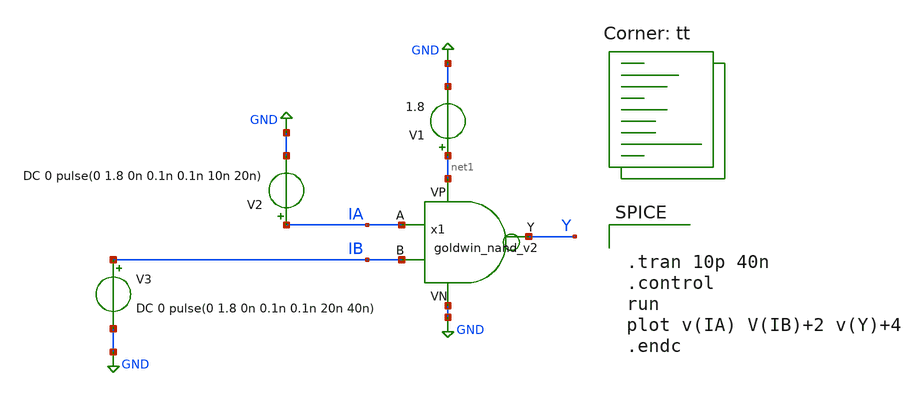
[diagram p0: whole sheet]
** sch_path: APIC-UTS/schematic/goldwin_nand_v2/tb_goldwin_nand_v2.sch
**.subckt tb_goldwin_nand_v2
V1 net1 GND 1.8
V2 IA GND DC 0 pulse(0 1.8 0n 0.1n 0.1n 10n 20n)
V3 IB GND DC 0 pulse(0 1.8 0n 0.1n 0.1n 20n 40n)
x1 IA IB Y net1 GND goldwin_nand_v2
**** begin user architecture code


.tran 10p 40n
.control
run
plot v(IA) V(IB)+2 v(Y)+4
.endc


.lib $::SKYWATER_MODELS/sky130.lib.spice tt
**** end user architecture code
**.ends

* expanding   symbol:  goldwin_nand_v2.sym # of pins=5
** sym_path: APIC-UTS/schematic/goldwin_nand_v2/goldwin_nand_v2.sym
** sch_path: APIC-UTS/schematic/goldwin_nand_v2/goldwin_nand_v2.sch
.subckt goldwin_nand_v2 A B Y VP VN
*.ipin A
*.ipin B
*.ipin VP
*.ipin VN
*.opin Y
XM1 Y A VP VP sky130_fd_pr__pfet_01v8 L=0.15 W=3 nf=1 ad='int((nf+1)/2) * W/nf * 0.29' as='int((nf+2)/2) * W/nf * 0.29'
+ pd='2*int((nf+1)/2) * (W/nf + 0.29)' ps='2*int((nf+2)/2) * (W/nf + 0.29)' nrd='0.29 / W' nrs='0.29 / W'
+ sa=0 sb=0 sd=0 mult=1 m=1
XM2 Y B VP VP sky130_fd_pr__pfet_01v8 L=0.15 W=3 nf=1 ad='int((nf+1)/2) * W/nf * 0.29' as='int((nf+2)/2) * W/nf * 0.29'
+ pd='2*int((nf+1)/2) * (W/nf + 0.29)' ps='2*int((nf+2)/2) * (W/nf + 0.29)' nrd='0.29 / W' nrs='0.29 / W'
+ sa=0 sb=0 sd=0 mult=1 m=1
XM3 Y B net1 VN sky130_fd_pr__nfet_01v8 L=0.15 W=1 nf=1 ad='int((nf+1)/2) * W/nf * 0.29' as='int((nf+2)/2) * W/nf * 0.29'
+ pd='2*int((nf+1)/2) * (W/nf + 0.29)' ps='2*int((nf+2)/2) * (W/nf + 0.29)' nrd='0.29 / W' nrs='0.29 / W'
+ sa=0 sb=0 sd=0 mult=1 m=1
XM4 net1 A VN VN sky130_fd_pr__nfet_01v8 L=0.15 W=1 nf=1 ad='int((nf+1)/2) * W/nf * 0.29' as='int((nf+2)/2) * W/nf * 0.29'
+ pd='2*int((nf+1)/2) * (W/nf + 0.29)' ps='2*int((nf+2)/2) * (W/nf + 0.29)' nrd='0.29 / W' nrs='0.29 / W'
+ sa=0 sb=0 sd=0 mult=1 m=1
.ends

.GLOBAL GND
.end
